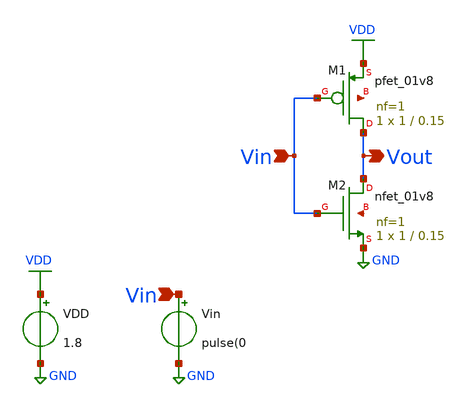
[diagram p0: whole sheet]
** sch_path: xschem/untitled.sch
**.subckt untitled Vin Vin Vout
*.ipin Vin
*.ipin Vin
*.opin Vout
VDD VDD GND 1.8
Vin Vin GND pulse(0
XM1 Vout Vin VDD net1 sky130_fd_pr__pfet_01v8 L=0.15 W=1 nf=1 ad='int((nf+1)/2) * W/nf * 0.29' as='int((nf+2)/2) * W/nf * 0.29'
+ pd='2*int((nf+1)/2) * (W/nf + 0.29)' ps='2*int((nf+2)/2) * (W/nf + 0.29)' nrd='0.29 / W' nrs='0.29 / W'
+ sa=0 sb=0 sd=0 mult=1 m=1
XM2 Vout Vin GND net2 sky130_fd_pr__nfet_01v8 L=0.15 W=1 nf=1 ad='int((nf+1)/2) * W/nf * 0.29' as='int((nf+2)/2) * W/nf * 0.29'
+ pd='2*int((nf+1)/2) * (W/nf + 0.29)' ps='2*int((nf+2)/2) * (W/nf + 0.29)' nrd='0.29 / W' nrs='0.29 / W'
+ sa=0 sb=0 sd=0 mult=1 m=1
**** begin user architecture code

blabla

**** end user architecture code
**.ends
.GLOBAL VDD
.GLOBAL GND
.end
